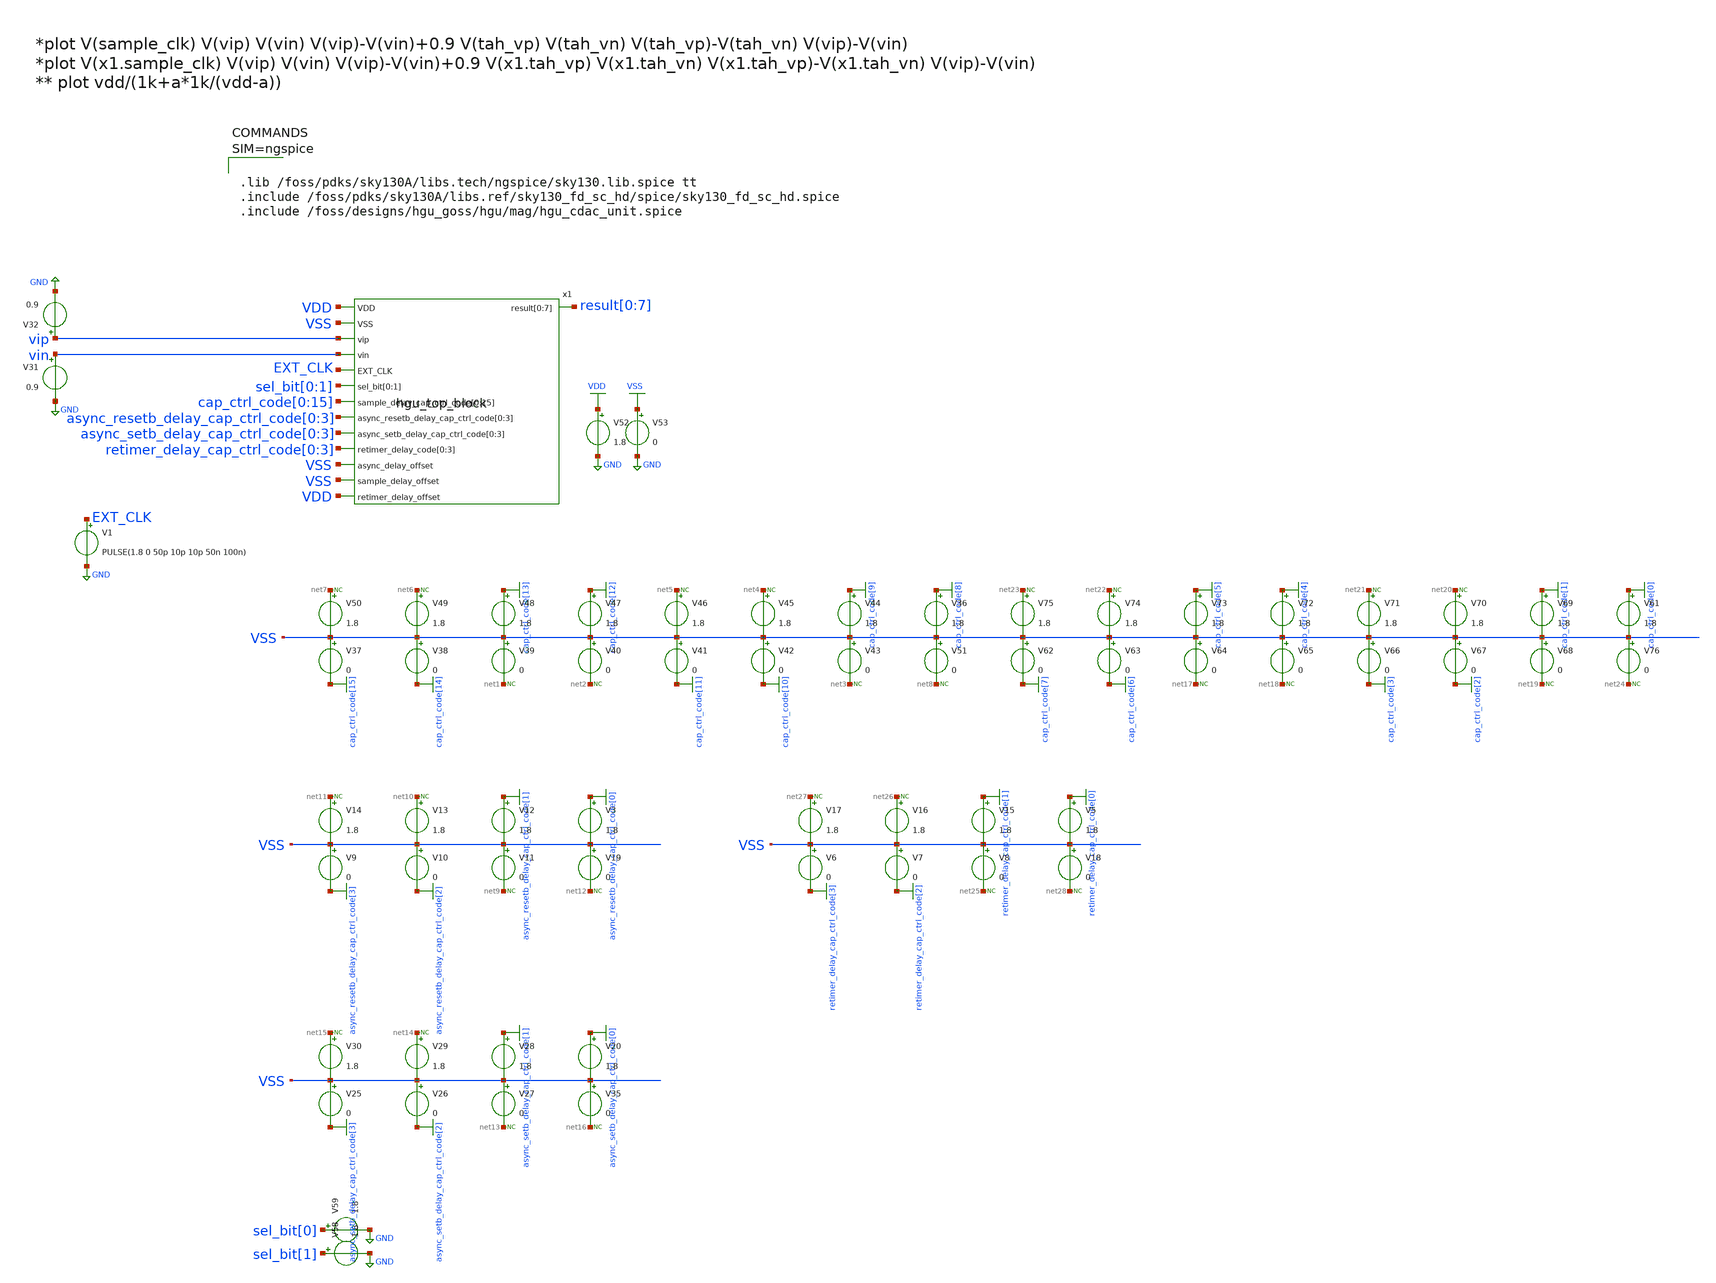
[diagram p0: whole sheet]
** sch_path: hgu/xschem/tb_hgu_top_block.sch
**.subckt tb_hgu_top_block
x1 VDD result[0] result[1] result[2] result[3] result[4] result[5] result[6] result[7] VSS vip vin
+ EXT_CLK sel_bit[0] sel_bit[1] cap_ctrl_code[0] cap_ctrl_code[1] cap_ctrl_code[2] cap_ctrl_code[3]
+ cap_ctrl_code[4] cap_ctrl_code[5] cap_ctrl_code[6] cap_ctrl_code[7] cap_ctrl_code[8] cap_ctrl_code[9]
+ cap_ctrl_code[10] cap_ctrl_code[11] cap_ctrl_code[12] cap_ctrl_code[13] cap_ctrl_code[14] cap_ctrl_code[15]
+ async_resetb_delay_cap_ctrl_code[0] async_resetb_delay_cap_ctrl_code[1] async_resetb_delay_cap_ctrl_code[2]
+ async_resetb_delay_cap_ctrl_code[3] async_setb_delay_cap_ctrl_code[0] async_setb_delay_cap_ctrl_code[1]
+ async_setb_delay_cap_ctrl_code[2] async_setb_delay_cap_ctrl_code[3] retimer_delay_cap_ctrl_code[0] retimer_delay_cap_ctrl_code[1]
+ retimer_delay_cap_ctrl_code[2] retimer_delay_cap_ctrl_code[3] VSS VSS VDD hgu_top_block
V36 cap_ctrl_code[8] VSS 1.8
V37 VSS cap_ctrl_code[15] 0
V38 VSS cap_ctrl_code[14] 0
V39 VSS net1 0
V40 VSS net2 0
V41 VSS cap_ctrl_code[11] 0
V42 VSS cap_ctrl_code[10] 0
V43 VSS net3 0
V44 cap_ctrl_code[9] VSS 1.8
V45 net4 VSS 1.8
V46 net5 VSS 1.8
V47 cap_ctrl_code[12] VSS 1.8
V48 cap_ctrl_code[13] VSS 1.8
V49 net6 VSS 1.8
V50 net7 VSS 1.8
V51 VSS net8 0
* noconn #net7
* noconn #net6
* noconn #net1
* noconn #net2
* noconn #net5
* noconn #net4
* noconn #net3
* noconn #net8
V52 VDD GND 1.8
V53 VSS GND 0
V58 sel_bit[1] GND 1.8
V59 sel_bit[0] GND 1.8
V3 async_resetb_delay_cap_ctrl_code[0] VSS 1.8
V9 VSS async_resetb_delay_cap_ctrl_code[3] 0
V10 VSS async_resetb_delay_cap_ctrl_code[2] 0
V11 VSS net9 0
V12 async_resetb_delay_cap_ctrl_code[1] VSS 1.8
V13 net10 VSS 1.8
V14 net11 VSS 1.8
V19 VSS net12 0
* noconn #net11
* noconn #net10
* noconn #net9
* noconn #net12
V20 async_setb_delay_cap_ctrl_code[0] VSS 1.8
V25 VSS async_setb_delay_cap_ctrl_code[3] 0
V26 VSS async_setb_delay_cap_ctrl_code[2] 0
V27 VSS net13 0
V28 async_setb_delay_cap_ctrl_code[1] VSS 1.8
V29 net14 VSS 1.8
V30 net15 VSS 1.8
V35 VSS net16 0
* noconn #net15
* noconn #net14
* noconn #net13
* noconn #net16
V61 cap_ctrl_code[0] VSS 1.8
V62 VSS cap_ctrl_code[7] 0
V63 VSS cap_ctrl_code[6] 0
V64 VSS net17 0
V65 VSS net18 0
V66 VSS cap_ctrl_code[3] 0
V67 VSS cap_ctrl_code[2] 0
V68 VSS net19 0
V69 cap_ctrl_code[1] VSS 1.8
V70 net20 VSS 1.8
V71 net21 VSS 1.8
V72 cap_ctrl_code[4] VSS 1.8
V73 cap_ctrl_code[5] VSS 1.8
V74 net22 VSS 1.8
V75 net23 VSS 1.8
V76 VSS net24 0
* noconn #net23
* noconn #net22
* noconn #net17
* noconn #net18
* noconn #net21
* noconn #net20
* noconn #net19
* noconn #net24
V5 retimer_delay_cap_ctrl_code[0] VSS 1.8
V6 VSS retimer_delay_cap_ctrl_code[3] 0
V7 VSS retimer_delay_cap_ctrl_code[2] 0
V8 VSS net25 0
V15 retimer_delay_cap_ctrl_code[1] VSS 1.8
V16 net26 VSS 1.8
V17 net27 VSS 1.8
V18 VSS net28 0
* noconn #net27
* noconn #net26
* noconn #net25
* noconn #net28
V31 vin GND 0.9
V32 vip GND 0.9
V1 EXT_CLK GND PULSE(1.8 0 50p 10p 10p 50n 100n)
**** begin user architecture code



.tran 10ps 250ns

.control
	run
	let pow = i(v52) * v(vdd) * -1
	meas tran sar_adc_avg_pow avg pow from=150n to=250n
.endc
.save all






.lib /foss/pdks/sky130A/libs.tech/ngspice/sky130.lib.spice tt
.include /foss/pdks/sky130A/libs.ref/sky130_fd_sc_hd/spice/sky130_fd_sc_hd.spice
.include /foss/designs/hgu_goss/hgu/mag/hgu_cdac_unit.spice



**** end user architecture code
**.ends
.GLOBAL cap_ctrl_code[15]
.GLOBAL cap_ctrl_code[14]
.GLOBAL cap_ctrl_code[13]
.GLOBAL cap_ctrl_code[12]
.GLOBAL cap_ctrl_code[11]
.GLOBAL cap_ctrl_code[10]
.GLOBAL cap_ctrl_code[9]
.GLOBAL cap_ctrl_code[8]
.GLOBAL VDD
.GLOBAL GND
.GLOBAL VSS
.GLOBAL async_resetb_delay_cap_ctrl_code[3]
.GLOBAL async_resetb_delay_cap_ctrl_code[2]
.GLOBAL async_resetb_delay_cap_ctrl_code[1]
.GLOBAL async_resetb_delay_cap_ctrl_code[0]
.GLOBAL async_setb_delay_cap_ctrl_code[3]
.GLOBAL async_setb_delay_cap_ctrl_code[2]
.GLOBAL async_setb_delay_cap_ctrl_code[1]
.GLOBAL async_setb_delay_cap_ctrl_code[0]
.GLOBAL cap_ctrl_code[7]
.GLOBAL cap_ctrl_code[6]
.GLOBAL cap_ctrl_code[5]
.GLOBAL cap_ctrl_code[4]
.GLOBAL cap_ctrl_code[3]
.GLOBAL cap_ctrl_code[2]
.GLOBAL cap_ctrl_code[1]
.GLOBAL cap_ctrl_code[0]
.GLOBAL retimer_delay_cap_ctrl_code[3]
.GLOBAL retimer_delay_cap_ctrl_code[2]
.GLOBAL retimer_delay_cap_ctrl_code[1]
.GLOBAL retimer_delay_cap_ctrl_code[0]
.end
